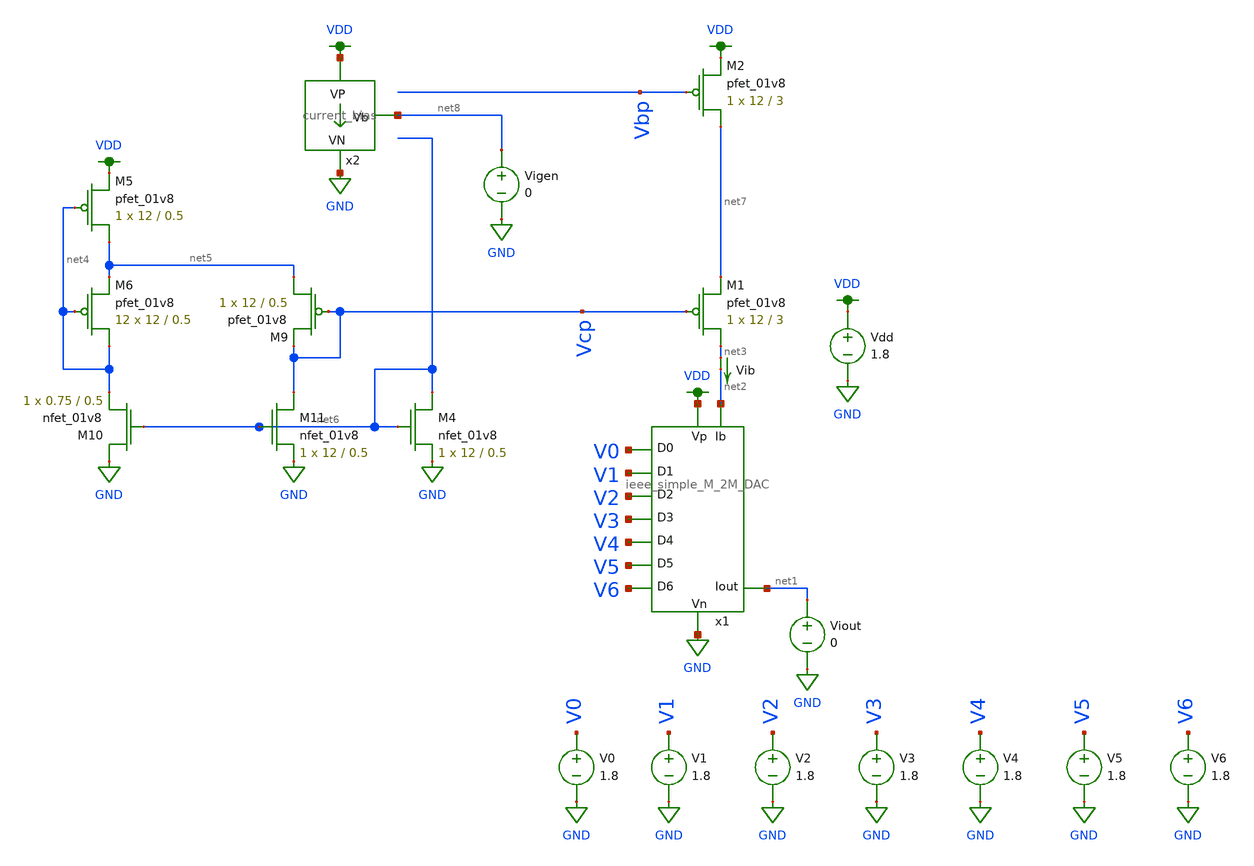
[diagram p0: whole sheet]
** sch_path: schematics/ieee DAC/ieee_DAC_mc_simulation_2.sch
**.subckt ieee_DAC_mc_simulation_2
Vdd VDD GND 1.8
V1 V1 GND 1.8
V2 V2 GND 1.8
V3 V3 GND 1.8
V4 V4 GND 1.8
V5 V5 GND 1.8
V6 V6 GND 1.8
V0 V0 GND 1.8
Viout net1 GND 0
Vib net3 net2 0
.save i(vib)
x1 VDD net1 GND V1 V0 V2 V3 V4 V5 V6 net2 ieee_simple_M_2M_DAC
XM1 net3 Vcp net7 VDD sky130_fd_pr__pfet_01v8 L=3 W=12 nf=1 ad='int((nf+1)/2) * W/nf * 0.29' as='int((nf+2)/2) * W/nf * 0.29'
+ pd='2*int((nf+1)/2) * (W/nf + 0.29)' ps='2*int((nf+2)/2) * (W/nf + 0.29)' nrd='0.29 / W' nrs='0.29 / W'
+ sa=0 sb=0 sd=0 mult=1 m=1
XM5 net5 net4 VDD VDD sky130_fd_pr__pfet_01v8 L=0.5 W=12 nf=1 ad='int((nf+1)/2) * W/nf * 0.29' as='int((nf+2)/2) * W/nf * 0.29'
+ pd='2*int((nf+1)/2) * (W/nf + 0.29)' ps='2*int((nf+2)/2) * (W/nf + 0.29)' nrd='0.29 / W' nrs='0.29 / W'
+ sa=0 sb=0 sd=0 mult=1 m=1
XM6 net4 net4 net5 VDD sky130_fd_pr__pfet_01v8 L=0.5 W=12 nf=1 ad='int((nf+1)/2) * W/nf * 0.29' as='int((nf+2)/2) * W/nf * 0.29'
+ pd='2*int((nf+1)/2) * (W/nf + 0.29)' ps='2*int((nf+2)/2) * (W/nf + 0.29)' nrd='0.29 / W' nrs='0.29 / W'
+ sa=0 sb=0 sd=0 mult=12 m=12
XM9 net5 Vcp Vcp VDD sky130_fd_pr__pfet_01v8 L=0.5 W=12 nf=1 ad='int((nf+1)/2) * W/nf * 0.29' as='int((nf+2)/2) * W/nf * 0.29'
+ pd='2*int((nf+1)/2) * (W/nf + 0.29)' ps='2*int((nf+2)/2) * (W/nf + 0.29)' nrd='0.29 / W' nrs='0.29 / W'
+ sa=0 sb=0 sd=0 mult=1 m=1
XM10 GND net6 net4 GND sky130_fd_pr__nfet_01v8 L=0.5 W=0.75 nf=1 ad='int((nf+1)/2) * W/nf * 0.29' as='int((nf+2)/2) * W/nf * 0.29'
+ pd='2*int((nf+1)/2) * (W/nf + 0.29)' ps='2*int((nf+2)/2) * (W/nf + 0.29)' nrd='0.29 / W' nrs='0.29 / W'
+ sa=0 sb=0 sd=0 mult=1 m=1
XM11 Vcp net6 GND GND sky130_fd_pr__nfet_01v8 L=0.5 W=12 nf=1 ad='int((nf+1)/2) * W/nf * 0.29' as='int((nf+2)/2) * W/nf * 0.29'
+ pd='2*int((nf+1)/2) * (W/nf + 0.29)' ps='2*int((nf+2)/2) * (W/nf + 0.29)' nrd='0.29 / W' nrs='0.29 / W'
+ sa=0 sb=0 sd=0 mult=1 m=1
XM2 net7 Vbp VDD VDD sky130_fd_pr__pfet_01v8 L=3 W=12 nf=1 ad='int((nf+1)/2) * W/nf * 0.29' as='int((nf+2)/2) * W/nf * 0.29'
+ pd='2*int((nf+1)/2) * (W/nf + 0.29)' ps='2*int((nf+2)/2) * (W/nf + 0.29)' nrd='0.29 / W' nrs='0.29 / W'
+ sa=0 sb=0 sd=0 mult=1 m=1
XM4 net6 net6 GND GND sky130_fd_pr__nfet_01v8 L=0.5 W=12 nf=1 ad='int((nf+1)/2) * W/nf * 0.29' as='int((nf+2)/2) * W/nf * 0.29'
+ pd='2*int((nf+1)/2) * (W/nf + 0.29)' ps='2*int((nf+2)/2) * (W/nf + 0.29)' nrd='0.29 / W' nrs='0.29 / W'
+ sa=0 sb=0 sd=0 mult=1 m=1
x2 VDD net8 GND current_bias
Vigen net8 GND 0
**** begin user architecture code

.option wnflag=1
.param MC_SWITCH=1.0
.lib ~/skywater/skywater-pdk/libraries/sky130_fd_pr_ngspice/latest/models/sky130.lib.spice tt


.save all
.control
set wr_vecnames
set wr_singlescale

let Ibias_max = 31n
let Ibias = 30n
dowhile Ibias < Ibias_max
alter Ib $&Ibias

let mc_runs = 10
let run = 1
dowhile run <= mc_runs

  let code = 0
  while code < 128
    if floor(code / 1) eq 0
      let b0 = 0
    else
      let b0 = (floor(code / 1) % 2) * 1.8
    end
    if floor(code / 2) eq 0
      let b1 = 0
    else
      let b1 = (floor(code / 2) % 2) * 1.8
    end
    if floor(code / 4) eq 0
      let b2 = 0
    else
      let b2 = (floor(code / 4) % 2) * 1.8
    end
    if floor(code / 8) eq 0
      let b3 = 0
    else
      let b3 = (floor(code / 8) % 2) * 1.8
    end
    if floor(code / 16) eq 0
      let b4 = 0
    else
      let b4 = (floor(code / 16) % 2) * 1.8
    end
    if floor(code / 32) eq 0
      let b5 = 0
    else
      let b5 = (floor(code / 32) % 2) * 1.8
    end
    if floor(code / 64) eq 0
      let b6 = 0
    else
      let b6 = (floor(code / 64) % 2) * 1.8
    end

    alter V0 $&b0
    alter V1 $&b1
    alter V2 $&b2
    alter V3 $&b3
    alter V4 $&b4
    alter V5 $&b5
    alter V6 $&b6
    save all
    op

    wrdata ~/dev/git/7-bit-D-A-converter-MP4-MADVLSI/schematics/simulations/ieee_DAC/dac_with_external_bias_gen/test_6/ieeeDAC_{$&run}.txt
+ V0 V1 V2 V3 V4 V5 V6 i(Vib) i(Viout)
    if code eq 0
      set appendwrite
      set wr_vecnames = FALSE
    end
    let code = code + 1
  end
  reset
  set appendwrite = FALSE
  set wr_vecnames
  let run = run + 1
end

let Ibias = Ibias * 2
end
.endc

**** end user architecture code
**.ends
.GLOBAL VDD
.GLOBAL GND
.end
